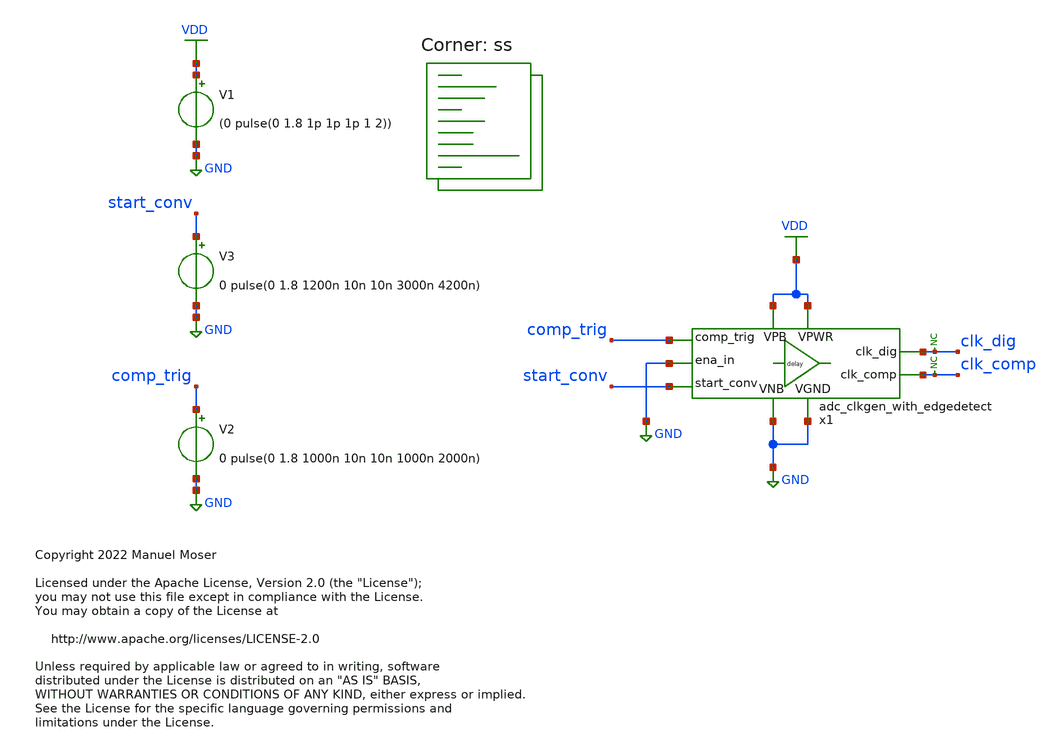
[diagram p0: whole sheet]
** sch_path: openlane/adc_clkgen_with_edgedetect/runs/kasleberkas/postlayoutsim/adc_clkgen_with_edgedetect_tb.sch
* Copyright 2022 Manuel Moser
* Licensed under the Apache License, Version 2.0 (the "License");
**.subckt adc_clkgen_with_edgedetect_tb
V1 VDD GND (0 pulse(0 1.8 1p 1p 1p 1 2))
V2 comp_trig GND 0 pulse(0 1.8 1000n 10n 10n 1000n 2000n)
* noconn clk_dig
x1 VDD GND clk_dig GND VDD GND comp_trig start_conv clk_comp adc_clkgen_with_edgedetect
* noconn clk_comp
V3 start_conv GND 0 pulse(0 1.8 1200n 10n 10n 3000n 4200n)
**** begin user architecture code

*.include /foss/pdk/sky130A/libs.ref/sky130_fd_sc_hd/spice/sky130_fd_sc_hd.spice
.include /foss/designs/SKY130_SAR-ADC/openlane/adc_clkgen_with_edgedetect/runs/kasleberkas/postlayoutsim/adc_clkgen_with_edgedetect.spice
*.OPTIONS RELTOL=.001 TRTOL=1 ABSTOL=1e-16 CHGTOL=1.0e-16 DEFAD=1.0e-16
.save all
.control
tran 1n 5000n
plot v(comp_trig) v(clk_dig)
plot v(comp_trig) v(start_conv) v(clk_comp)
.endc

.lib $::SKYWATER_MODELS/sky130.lib.spice ss
**** end user architecture code
**.ends
.GLOBAL VDD
.GLOBAL GND
.end
